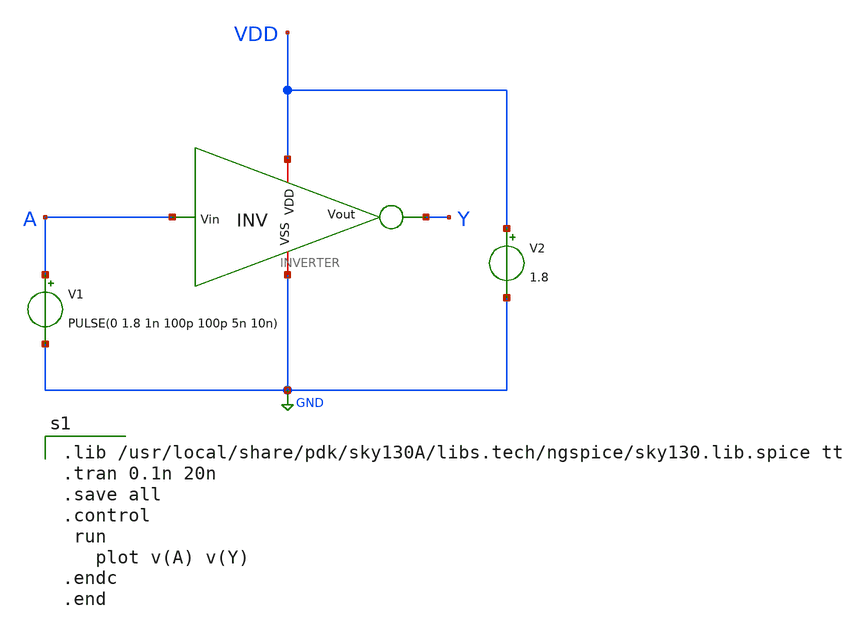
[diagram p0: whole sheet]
** sch_path: INVERTER/INVERTER_SIM.sch
**.subckt INVERTER_SIM
x1 VDD A Y GND INVERTER
V1 A GND PULSE(0 1.8 1n 100p 100p 5n 10n)
V2 VDD GND 1.8
**** begin user architecture code

.lib /usr/local/share/pdk/sky130A/libs.tech/ngspice/sky130.lib.spice tt
.tran 0.1n 20n
.save all
.control
 run
   plot v(A) v(Y)
.endc
.end


**** end user architecture code
**.ends
.GLOBAL GND
.end
